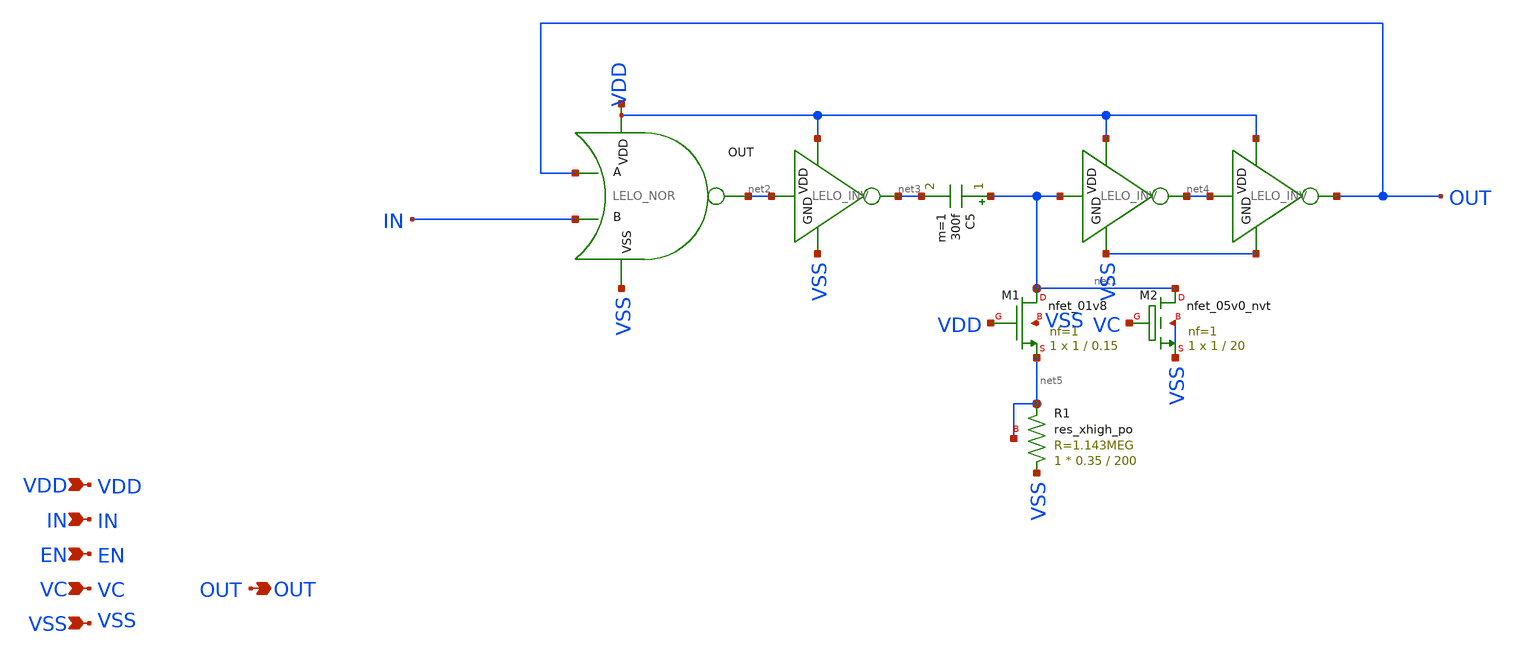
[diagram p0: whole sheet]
** sch_path: design/LELO_SVOD_SKY130A/LELO_ONESHOT_VC2.sch
**.subckt LELO_ONESHOT_VC2 VDD IN VC VSS OUT EN
*.ipin VDD
*.ipin IN
*.ipin VC
*.ipin VSS
*.opin OUT
*.ipin EN
x2 net6 net2 OUT IN VSS LELO_NOR
C5 net1 net3 300f m=1
x3 VDD net1 net4 VSS LELO_INV
x1 VDD net2 net3 VSS LELO_INV
x4 VDD net4 OUT VSS LELO_INV
XM2 net1 VC VSS VSS sky130_fd_pr__nfet_05v0_nvt L=20 W=1 nf=1 ad='int((1 + 1)/2) * 1 / 1 * 0.29' as='int((1 + 2)/2) * 1 / 1 * 0.29'
+ pd='2*int((1 + 1)/2) * (1 / 1 + 0.29)' ps='2*int((1 + 2)/2) * (1 / 1 + 0.29)' nrd='0.29 / 1 ' nrs='0.29 / 1 '
+ sa=0 sb=0 sd=0 mult=1 m=1
XR1 VSS net5 net5 sky130_fd_pr__res_xhigh_po W=0.35 L=200 mult=1 m=1
XM1 net1 VDD net5 VSS sky130_fd_pr__nfet_01v8 L=0.15 W=1 nf=1 ad='int((1 + 1)/2) * 1 / 1 * 0.29' as='int((1 + 2)/2) * 1 / 1 * 0.29'
+ pd='2*int((1 + 1)/2) * (1 / 1 + 0.29)' ps='2*int((1 + 2)/2) * (1 / 1 + 0.29)' nrd='0.29 / 1 ' nrs='0.29 / 1 '
+ sa=0 sb=0 sd=0 mult=1 m=1
**.ends

* expanding   symbol:  LELO_SVOD_SKY130A/LELO_NOR.sym # of pins=5
** sym_path: design/LELO_SVOD_SKY130A/LELO_NOR.sym
** sch_path: design/LELO_SVOD_SKY130A/LELO_NOR.sch
.subckt LELO_NOR VDD OUT A B VSS
*.ipin VDD
*.ipin VSS
*.opin OUT
*.ipin A
*.ipin B
XM2 OUT B VSS VSS sky130_fd_pr__nfet_01v8 L=0.15 W=2 nf=1 ad='int((1 + 1)/2) * 2 / 1 * 0.29' as='int((1 + 2)/2) * 2 / 1 * 0.29'
+ pd='2*int((1 + 1)/2) * (2 / 1 + 0.29)' ps='2*int((1 + 2)/2) * (2 / 1 + 0.29)' nrd='0.29 / 2 ' nrs='0.29 / 2 '
+ sa=0 sb=0 sd=0 mult=1 m=1
XM1 OUT A VSS VSS sky130_fd_pr__nfet_01v8 L=0.15 W=2 nf=1 ad='int((1 + 1)/2) * 2 / 1 * 0.29' as='int((1 + 2)/2) * 2 / 1 * 0.29'
+ pd='2*int((1 + 1)/2) * (2 / 1 + 0.29)' ps='2*int((1 + 2)/2) * (2 / 1 + 0.29)' nrd='0.29 / 2 ' nrs='0.29 / 2 '
+ sa=0 sb=0 sd=0 mult=1 m=1
XM3 OUT B net1 VDD sky130_fd_pr__pfet_01v8 L=0.15 W=4 nf=1 ad='int((1 + 1)/2) * 4 / 1 * 0.29' as='int((1 + 2)/2) * 4 / 1 * 0.29'
+ pd='2*int((1 + 1)/2) * (4 / 1 + 0.29)' ps='2*int((1 + 2)/2) * (4 / 1 + 0.29)' nrd='0.29 / 4 ' nrs='0.29 / 4 '
+ sa=0 sb=0 sd=0 mult=1 m=1
XM4 net1 A VDD VDD sky130_fd_pr__pfet_01v8 L=0.15 W=4 nf=1 ad='int((1 + 1)/2) * 4 / 1 * 0.29' as='int((1 + 2)/2) * 4 / 1 * 0.29'
+ pd='2*int((1 + 1)/2) * (4 / 1 + 0.29)' ps='2*int((1 + 2)/2) * (4 / 1 + 0.29)' nrd='0.29 / 4 ' nrs='0.29 / 4 '
+ sa=0 sb=0 sd=0 mult=1 m=1
.ends


* expanding   symbol:  LELO_SVOD_SKY130A/LELO_INV.sym # of pins=4
** sym_path: design/LELO_SVOD_SKY130A/LELO_INV.sym
** sch_path: design/LELO_SVOD_SKY130A/LELO_INV.sch
.subckt LELO_INV VDD VIN VOUT GND
*.ipin VIN
*.ipin VDD
*.ipin GND
*.opin VOUT
XM1 VOUT VIN GND GND sky130_fd_pr__nfet_01v8_lvt L=0.15 W=1 nf=1 ad='int((1 + 1)/2) * 1 / 1 * 0.29' as='int((1 + 2)/2) * 1 / 1 * 0.29'
+ pd='2*int((1 + 1)/2) * (1 / 1 + 0.29)' ps='2*int((1 + 2)/2) * (1 / 1 + 0.29)' nrd='0.29 / 1 ' nrs='0.29 / 1 '
+ sa=0 sb=0 sd=0 mult=1 m=1
XM2 VOUT VIN VDD VDD sky130_fd_pr__pfet_01v8_lvt L=0.35 W=1 nf=1 ad='int((1 + 1)/2) * 1 / 1 * 0.29' as='int((1 + 2)/2) * 1 / 1 * 0.29'
+ pd='2*int((1 + 1)/2) * (1 / 1 + 0.29)' ps='2*int((1 + 2)/2) * (1 / 1 + 0.29)' nrd='0.29 / 1 ' nrs='0.29 / 1 '
+ sa=0 sb=0 sd=0 mult=2 m=2
.ends

.end
